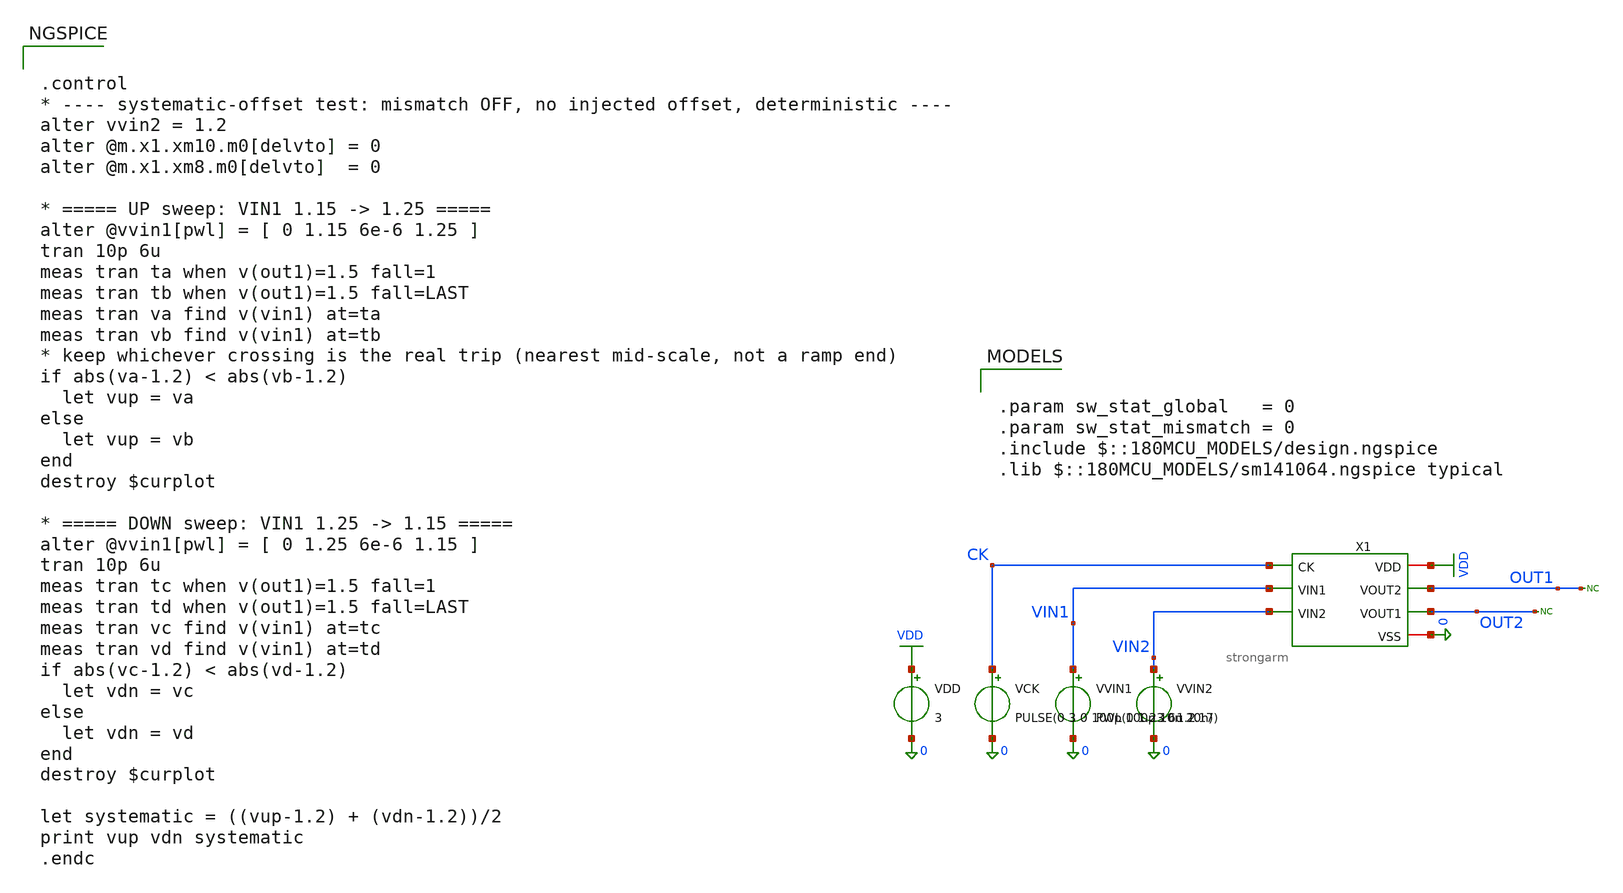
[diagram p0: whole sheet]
** sch_path: comparator/schematic/tests/strongarm_offset_measure_tb.sch
**.subckt strongarm_offset_measure_tb
X1 VDD CK OUT1 OUT2 VIN1 VIN2 0 strongarm
VVIN2 VIN2 0 1.2
VVIN1 VIN1 0 PWL(0 1.23 6u 1.17)
VDD VDD 0 3
VCK CK 0 PULSE(0 3 0 100p 100p 10n 20n)
* noconn OUT2
* noconn OUT1
**** begin user architecture code

.param sw_stat_global   = 0
.param sw_stat_mismatch = 0
.include $::180MCU_MODELS/design.ngspice
.lib $::180MCU_MODELS/sm141064.ngspice typical



.control
* ---- systematic-offset test: mismatch OFF, no injected offset, deterministic ----
alter vvin2 = 1.2
alter @m.x1.xm10.m0[delvto] = 0
alter @m.x1.xm8.m0[delvto]  = 0

* ===== UP sweep: VIN1 1.15 -> 1.25 =====
alter @vvin1[pwl] = [ 0 1.15 6e-6 1.25 ]
tran 10p 6u
meas tran ta when v(out1)=1.5 fall=1
meas tran tb when v(out1)=1.5 fall=LAST
meas tran va find v(vin1) at=ta
meas tran vb find v(vin1) at=tb
* keep whichever crossing is the real trip (nearest mid-scale, not a ramp end)
if abs(va-1.2) < abs(vb-1.2)
  let vup = va
else
  let vup = vb
end
destroy $curplot

* ===== DOWN sweep: VIN1 1.25 -> 1.15 =====
alter @vvin1[pwl] = [ 0 1.25 6e-6 1.15 ]
tran 10p 6u
meas tran tc when v(out1)=1.5 fall=1
meas tran td when v(out1)=1.5 fall=LAST
meas tran vc find v(vin1) at=tc
meas tran vd find v(vin1) at=td
if abs(vc-1.2) < abs(vd-1.2)
  let vdn = vc
else
  let vdn = vd
end
destroy $curplot

let systematic = ((vup-1.2) + (vdn-1.2))/2
print vup vdn systematic
.endc


**** end user architecture code
**.ends

* expanding   symbol:  comparator/schematic/strongarm.sym # of pins=7
** sym_path: comparator/schematic/strongarm.sym
** sch_path: comparator/schematic/strongarm.sch
.subckt strongarm VDD CK VOUT2 VOUT1 VIN1 VIN2 VSS
*.opin VOUT1
*.opin VOUT2
*.ipin VIN1
*.ipin VIN2
*.ipin CK
*.iopin VDD
*.iopin VSS
XM1 VOUT2 VOUT1 net1 net1 nfet_03v3 L=0.28u W=0.22u nf=1 ad='int((nf+1)/2) * W/nf * 0.18u' as='int((nf+2)/2) * W/nf * 0.18u'
+ pd='2*int((nf+1)/2) * (W/nf + 0.18u)' ps='2*int((nf+2)/2) * (W/nf + 0.18u)' nrd='0.18u / W' nrs='0.18u / W'
+ sa=0 sb=0 sd=0 m=1
XM2 VOUT1 VOUT2 VDD VDD pfet_03v3 L=0.28u W=0.22u nf=1 ad='int((nf+1)/2) * W/nf * 0.18u' as='int((nf+2)/2) * W/nf * 0.18u'
+ pd='2*int((nf+1)/2) * (W/nf + 0.18u)' ps='2*int((nf+2)/2) * (W/nf + 0.18u)' nrd='0.18u / W' nrs='0.18u / W'
+ sa=0 sb=0 sd=0 m=1
XM3 VOUT1 CK VDD VDD pfet_03v3 L=0.28u W=0.22u nf=1 ad='int((nf+1)/2) * W/nf * 0.18u' as='int((nf+2)/2) * W/nf * 0.18u'
+ pd='2*int((nf+1)/2) * (W/nf + 0.18u)' ps='2*int((nf+2)/2) * (W/nf + 0.18u)' nrd='0.18u / W' nrs='0.18u / W'
+ sa=0 sb=0 sd=0 m=1
XM4 net3 CK VDD VDD pfet_03v3 L=0.28u W=0.22u nf=1 ad='int((nf+1)/2) * W/nf * 0.18u' as='int((nf+2)/2) * W/nf * 0.18u'
+ pd='2*int((nf+1)/2) * (W/nf + 0.18u)' ps='2*int((nf+2)/2) * (W/nf + 0.18u)' nrd='0.18u / W' nrs='0.18u / W'
+ sa=0 sb=0 sd=0 m=1
XM5 net1 CK VDD VDD pfet_03v3 L=0.28u W=0.22u nf=1 ad='int((nf+1)/2) * W/nf * 0.18u' as='int((nf+2)/2) * W/nf * 0.18u'
+ pd='2*int((nf+1)/2) * (W/nf + 0.18u)' ps='2*int((nf+2)/2) * (W/nf + 0.18u)' nrd='0.18u / W' nrs='0.18u / W'
+ sa=0 sb=0 sd=0 m=1
XM6 VOUT2 CK VDD VDD pfet_03v3 L=0.28u W=0.22u nf=1 ad='int((nf+1)/2) * W/nf * 0.18u' as='int((nf+2)/2) * W/nf * 0.18u'
+ pd='2*int((nf+1)/2) * (W/nf + 0.18u)' ps='2*int((nf+2)/2) * (W/nf + 0.18u)' nrd='0.18u / W' nrs='0.18u / W'
+ sa=0 sb=0 sd=0 m=1
XM7 VOUT2 VOUT1 VDD VDD pfet_03v3 L=0.28u W=0.22u nf=1 ad='int((nf+1)/2) * W/nf * 0.18u' as='int((nf+2)/2) * W/nf * 0.18u'
+ pd='2*int((nf+1)/2) * (W/nf + 0.18u)' ps='2*int((nf+2)/2) * (W/nf + 0.18u)' nrd='0.18u / W' nrs='0.18u / W'
+ sa=0 sb=0 sd=0 m=1
XM8 net1 VIN2 net2 net2 nfet_03v3 L=0.28u W=0.22u nf=1 ad='int((nf+1)/2) * W/nf * 0.18u' as='int((nf+2)/2) * W/nf * 0.18u'
+ pd='2*int((nf+1)/2) * (W/nf + 0.18u)' ps='2*int((nf+2)/2) * (W/nf + 0.18u)' nrd='0.18u / W' nrs='0.18u / W'
+ sa=0 sb=0 sd=0 m=1
XM9 VOUT1 VOUT2 net3 net3 nfet_03v3 L=0.28u W=0.22u nf=1 ad='int((nf+1)/2) * W/nf * 0.18u' as='int((nf+2)/2) * W/nf * 0.18u'
+ pd='2*int((nf+1)/2) * (W/nf + 0.18u)' ps='2*int((nf+2)/2) * (W/nf + 0.18u)' nrd='0.18u / W' nrs='0.18u / W'
+ sa=0 sb=0 sd=0 m=1
XM10 net3 VIN1 net2 net2 nfet_03v3 L=0.28u W=0.22u nf=1 ad='int((nf+1)/2) * W/nf * 0.18u' as='int((nf+2)/2) * W/nf * 0.18u'
+ pd='2*int((nf+1)/2) * (W/nf + 0.18u)' ps='2*int((nf+2)/2) * (W/nf + 0.18u)' nrd='0.18u / W' nrs='0.18u / W'
+ sa=0 sb=0 sd=0 m=1
XM11 net2 CK VSS net2 nfet_03v3 L=0.28u W=0.22u nf=1 ad='int((nf+1)/2) * W/nf * 0.18u' as='int((nf+2)/2) * W/nf * 0.18u'
+ pd='2*int((nf+1)/2) * (W/nf + 0.18u)' ps='2*int((nf+2)/2) * (W/nf + 0.18u)' nrd='0.18u / W' nrs='0.18u / W'
+ sa=0 sb=0 sd=0 m=1
.ends

.GLOBAL VDD
.end
